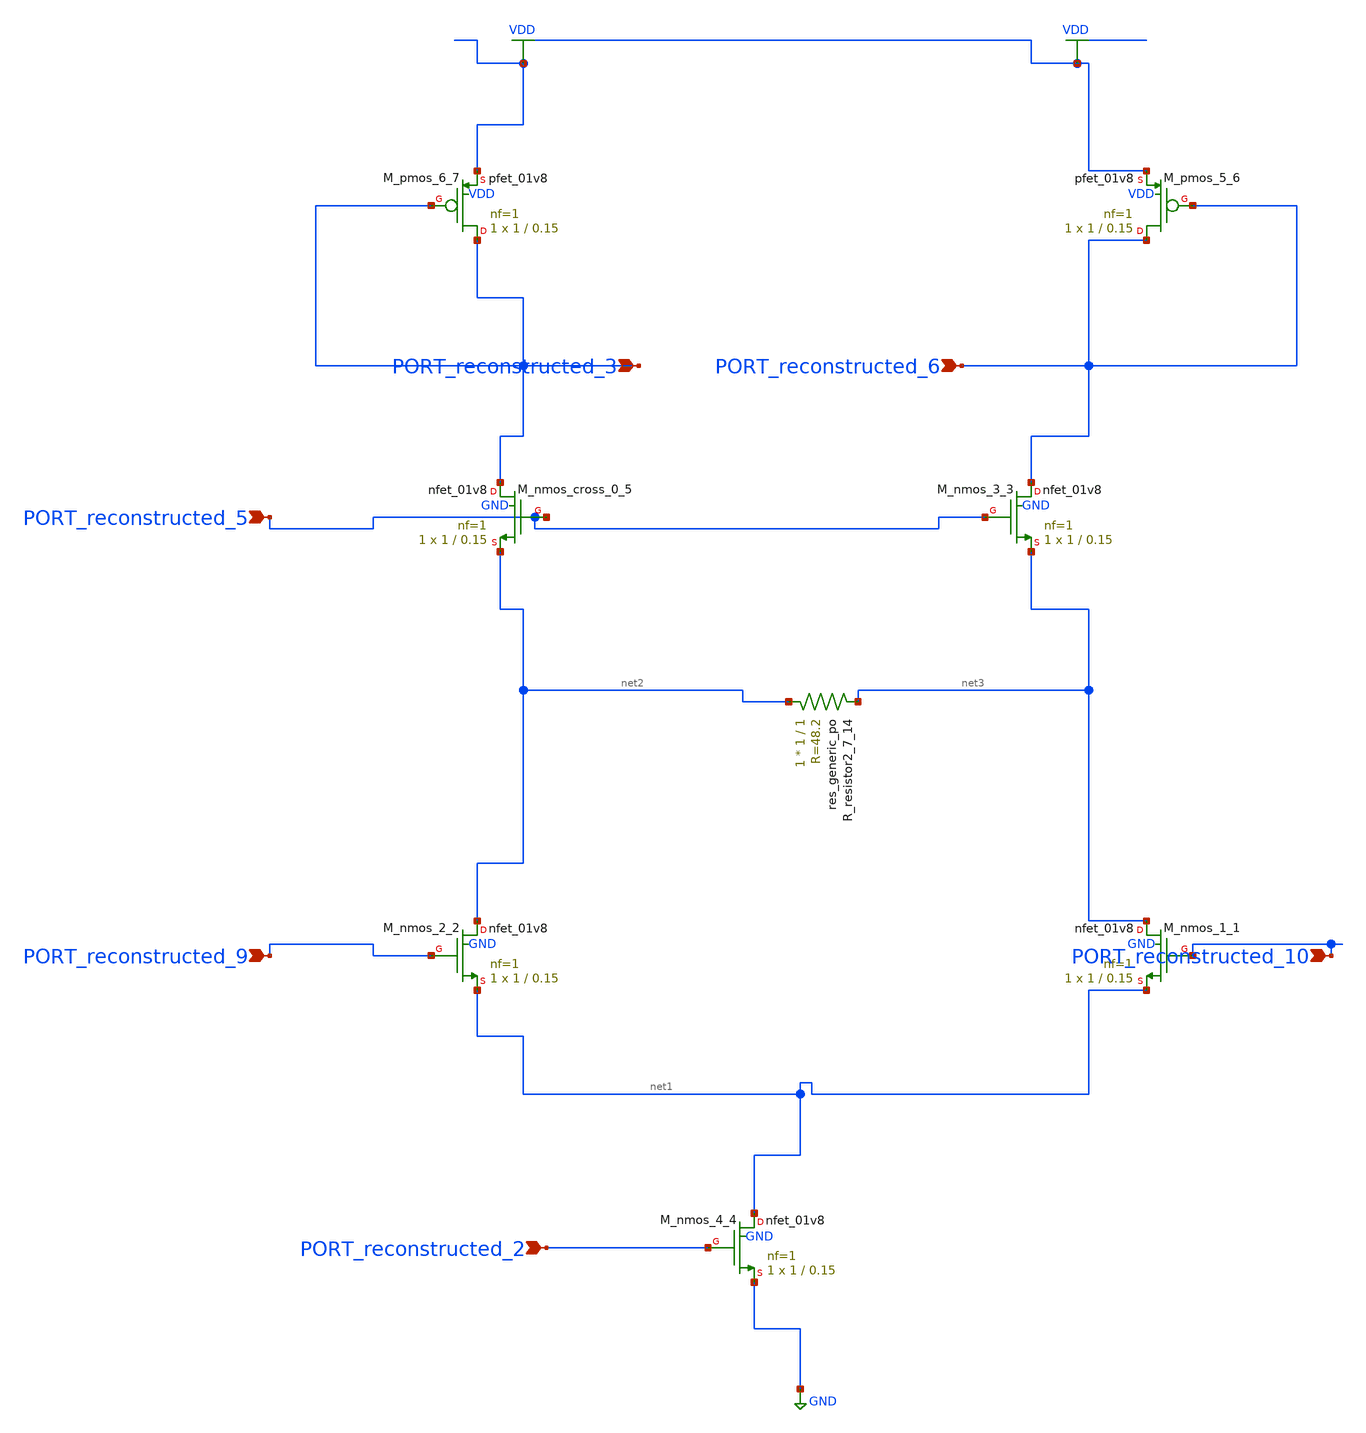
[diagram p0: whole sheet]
** sch_path: schematics/AMSNet/246.sch
**.subckt 246 PORT_reconstructed_9 PORT_reconstructed_6 PORT_reconstructed_2 PORT_reconstructed_3
*+ PORT_reconstructed_5 PORT_reconstructed_10
*.ipin PORT_reconstructed_9
*.ipin PORT_reconstructed_6
*.ipin PORT_reconstructed_2
*.ipin PORT_reconstructed_3
*.ipin PORT_reconstructed_5
*.ipin PORT_reconstructed_10
XM_nmos_1_1 net3 PORT_reconstructed_10 net1 GND sky130_fd_pr__nfet_01v8 L=0.15 W=1 nf=1 ad='int((1 + 1)/2) * 1 / 1 * 0.29'
+ as='int((1 + 2)/2) * 1 / 1 * 0.29' pd='2*int((1 + 1)/2) * (1 / 1 + 0.29)' ps='2*int((1 + 2)/2) * (1 / 1 + 0.29)'
+ nrd='0.29 / 1 ' nrs='0.29 / 1 ' sa=0 sb=0 sd=0 mult=1 m=1
XM_nmos_2_2 net2 PORT_reconstructed_9 net1 GND sky130_fd_pr__nfet_01v8 L=0.15 W=1 nf=1 ad='int((1 + 1)/2) * 1 / 1 * 0.29'
+ as='int((1 + 2)/2) * 1 / 1 * 0.29' pd='2*int((1 + 1)/2) * (1 / 1 + 0.29)' ps='2*int((1 + 2)/2) * (1 / 1 + 0.29)'
+ nrd='0.29 / 1 ' nrs='0.29 / 1 ' sa=0 sb=0 sd=0 mult=1 m=1
XM_nmos_3_3 PORT_reconstructed_6 PORT_reconstructed_5 net3 GND sky130_fd_pr__nfet_01v8 L=0.15 W=1 nf=1
+ ad='int((1 + 1)/2) * 1 / 1 * 0.29' as='int((1 + 2)/2) * 1 / 1 * 0.29' pd='2*int((1 + 1)/2) * (1 / 1 + 0.29)'
+ ps='2*int((1 + 2)/2) * (1 / 1 + 0.29)' nrd='0.29 / 1 ' nrs='0.29 / 1 ' sa=0 sb=0 sd=0 mult=1 m=1
XM_nmos_4_4 net1 PORT_reconstructed_2 GND GND sky130_fd_pr__nfet_01v8 L=0.15 W=1 nf=1 ad='int((1 + 1)/2) * 1 / 1 * 0.29'
+ as='int((1 + 2)/2) * 1 / 1 * 0.29' pd='2*int((1 + 1)/2) * (1 / 1 + 0.29)' ps='2*int((1 + 2)/2) * (1 / 1 + 0.29)'
+ nrd='0.29 / 1 ' nrs='0.29 / 1 ' sa=0 sb=0 sd=0 mult=1 m=1
XM_nmos_cross_0_5 PORT_reconstructed_3 PORT_reconstructed_5 net2 GND sky130_fd_pr__nfet_01v8 L=0.15 W=1
+ nf=1 ad='int((1 + 1)/2) * 1 / 1 * 0.29' as='int((1 + 2)/2) * 1 / 1 * 0.29' pd='2*int((1 + 1)/2) * (1 / 1 + 0.29)'
+ ps='2*int((1 + 2)/2) * (1 / 1 + 0.29)' nrd='0.29 / 1 ' nrs='0.29 / 1 ' sa=0 sb=0 sd=0 mult=1 m=1
XM_pmos_5_6 PORT_reconstructed_6 PORT_reconstructed_6 VDD VDD sky130_fd_pr__pfet_01v8 L=0.15 W=1 nf=1
+ ad='int((1 + 1)/2) * 1 / 1 * 0.29' as='int((1 + 2)/2) * 1 / 1 * 0.29' pd='2*int((1 + 1)/2) * (1 / 1 + 0.29)'
+ ps='2*int((1 + 2)/2) * (1 / 1 + 0.29)' nrd='0.29 / 1 ' nrs='0.29 / 1 ' sa=0 sb=0 sd=0 mult=1 m=1
XM_pmos_6_7 PORT_reconstructed_3 PORT_reconstructed_3 VDD VDD sky130_fd_pr__pfet_01v8 L=0.15 W=1 nf=1
+ ad='int((1 + 1)/2) * 1 / 1 * 0.29' as='int((1 + 2)/2) * 1 / 1 * 0.29' pd='2*int((1 + 1)/2) * (1 / 1 + 0.29)'
+ ps='2*int((1 + 2)/2) * (1 / 1 + 0.29)' nrd='0.29 / 1 ' nrs='0.29 / 1 ' sa=0 sb=0 sd=0 mult=1 m=1
XR_resistor2_7_14 net2 net3 sky130_fd_pr__res_generic_po W=1 L=1 m=1
**.ends
.GLOBAL GND
.GLOBAL VDD
.end
